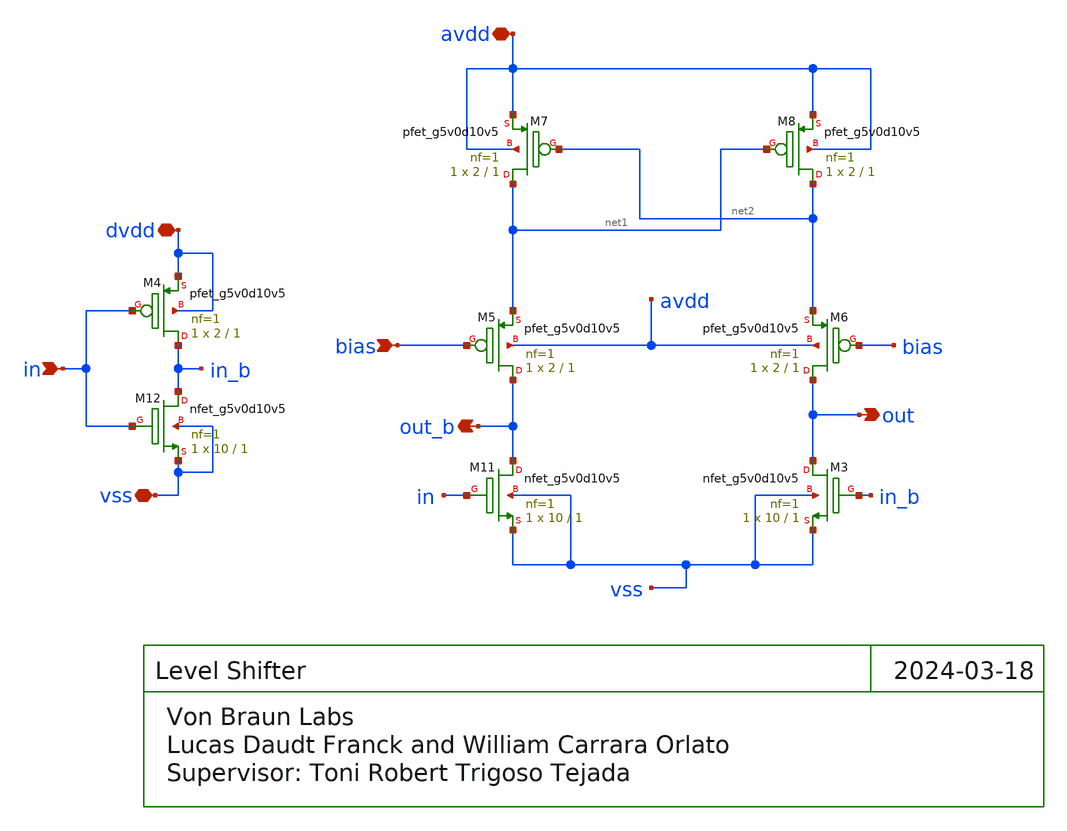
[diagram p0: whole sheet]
** sch_path: xschem/LevelShifter.sch
**.subckt LevelShifter in dvdd out out_b avdd bias vss
*.ipin in
*.iopin dvdd
*.opin out
*.opin out_b
*.iopin avdd
*.ipin bias
*.iopin vss
XM3 out in_b vss vss sky130_fd_pr__nfet_g5v0d10v5 L=1 W=10 nf=1 ad='int((nf+1)/2) * W/nf * 0.29' as='int((nf+2)/2) * W/nf * 0.29'
+ pd='2*int((nf+1)/2) * (W/nf + 0.29)' ps='2*int((nf+2)/2) * (W/nf + 0.29)' nrd='0.29 / W' nrs='0.29 / W'
+ sa=0 sb=0 sd=0 mult=1 m=1
XM4 in_b in dvdd dvdd sky130_fd_pr__pfet_g5v0d10v5 L=1 W=2 nf=1 ad='int((nf+1)/2) * W/nf * 0.29' as='int((nf+2)/2) * W/nf * 0.29'
+ pd='2*int((nf+1)/2) * (W/nf + 0.29)' ps='2*int((nf+2)/2) * (W/nf + 0.29)' nrd='0.29 / W' nrs='0.29 / W'
+ sa=0 sb=0 sd=0 mult=1 m=1
XM7 net1 net2 avdd avdd sky130_fd_pr__pfet_g5v0d10v5 L=1 W=2 nf=1 ad='int((nf+1)/2) * W/nf * 0.29' as='int((nf+2)/2) * W/nf * 0.29'
+ pd='2*int((nf+1)/2) * (W/nf + 0.29)' ps='2*int((nf+2)/2) * (W/nf + 0.29)' nrd='0.29 / W' nrs='0.29 / W'
+ sa=0 sb=0 sd=0 mult=1 m=1
XM8 net2 net1 avdd avdd sky130_fd_pr__pfet_g5v0d10v5 L=1 W=2 nf=1 ad='int((nf+1)/2) * W/nf * 0.29' as='int((nf+2)/2) * W/nf * 0.29'
+ pd='2*int((nf+1)/2) * (W/nf + 0.29)' ps='2*int((nf+2)/2) * (W/nf + 0.29)' nrd='0.29 / W' nrs='0.29 / W'
+ sa=0 sb=0 sd=0 mult=1 m=1
XM5 out_b bias net1 avdd sky130_fd_pr__pfet_g5v0d10v5 L=1 W=2 nf=1 ad='int((nf+1)/2) * W/nf * 0.29' as='int((nf+2)/2) * W/nf * 0.29'
+ pd='2*int((nf+1)/2) * (W/nf + 0.29)' ps='2*int((nf+2)/2) * (W/nf + 0.29)' nrd='0.29 / W' nrs='0.29 / W'
+ sa=0 sb=0 sd=0 mult=1 m=1
XM6 out bias net2 avdd sky130_fd_pr__pfet_g5v0d10v5 L=1 W=2 nf=1 ad='int((nf+1)/2) * W/nf * 0.29' as='int((nf+2)/2) * W/nf * 0.29'
+ pd='2*int((nf+1)/2) * (W/nf + 0.29)' ps='2*int((nf+2)/2) * (W/nf + 0.29)' nrd='0.29 / W' nrs='0.29 / W'
+ sa=0 sb=0 sd=0 mult=1 m=1
XM11 out_b in vss vss sky130_fd_pr__nfet_g5v0d10v5 L=1 W=10 nf=1 ad='int((nf+1)/2) * W/nf * 0.29' as='int((nf+2)/2) * W/nf * 0.29'
+ pd='2*int((nf+1)/2) * (W/nf + 0.29)' ps='2*int((nf+2)/2) * (W/nf + 0.29)' nrd='0.29 / W' nrs='0.29 / W'
+ sa=0 sb=0 sd=0 mult=1 m=1
XM12 in_b in vss vss sky130_fd_pr__nfet_g5v0d10v5 L=1 W=10 nf=1 ad='int((nf+1)/2) * W/nf * 0.29' as='int((nf+2)/2) * W/nf * 0.29'
+ pd='2*int((nf+1)/2) * (W/nf + 0.29)' ps='2*int((nf+2)/2) * (W/nf + 0.29)' nrd='0.29 / W' nrs='0.29 / W'
+ sa=0 sb=0 sd=0 mult=1 m=1
**.ends
.end
